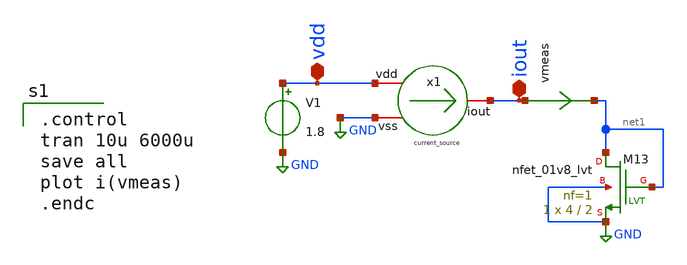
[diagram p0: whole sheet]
** sch_path: ANOTHER_SOLUTIONS_CONSIDERED/ANOTHER_BIAS_FOR_TEMPERATURE_SENSOR/CURRENT_SOURCE_FULL/XSCHEM/current_source_tb.sch
**.subckt current_source_tb iout vdd
*.iopin iout
*.iopin vdd
x1 vdd iout GND current_source
V1 vdd GND 1.8
XM13 net1 net1 GND GND sky130_fd_pr__nfet_01v8_lvt L=2 W=4 nf=1 ad='int((nf+1)/2) * W/nf * 0.29' as='int((nf+2)/2) * W/nf * 0.29'
+ pd='2*int((nf+1)/2) * (W/nf + 0.29)' ps='2*int((nf+2)/2) * (W/nf + 0.29)' nrd='0.29 / W' nrs='0.29 / W'
+ sa=0 sb=0 sd=0 mult=1 m=1
vmeas iout net1 0
.save i(vmeas)
**** begin user architecture code

.control
tran 10u 6000u
save all
plot i(vmeas)
.endc


** opencircuitdesign pdks install
.lib $::SKYWATER_MODELS/sky130.lib.spice tt


**** end user architecture code
**.ends
.GLOBAL GND
.end
